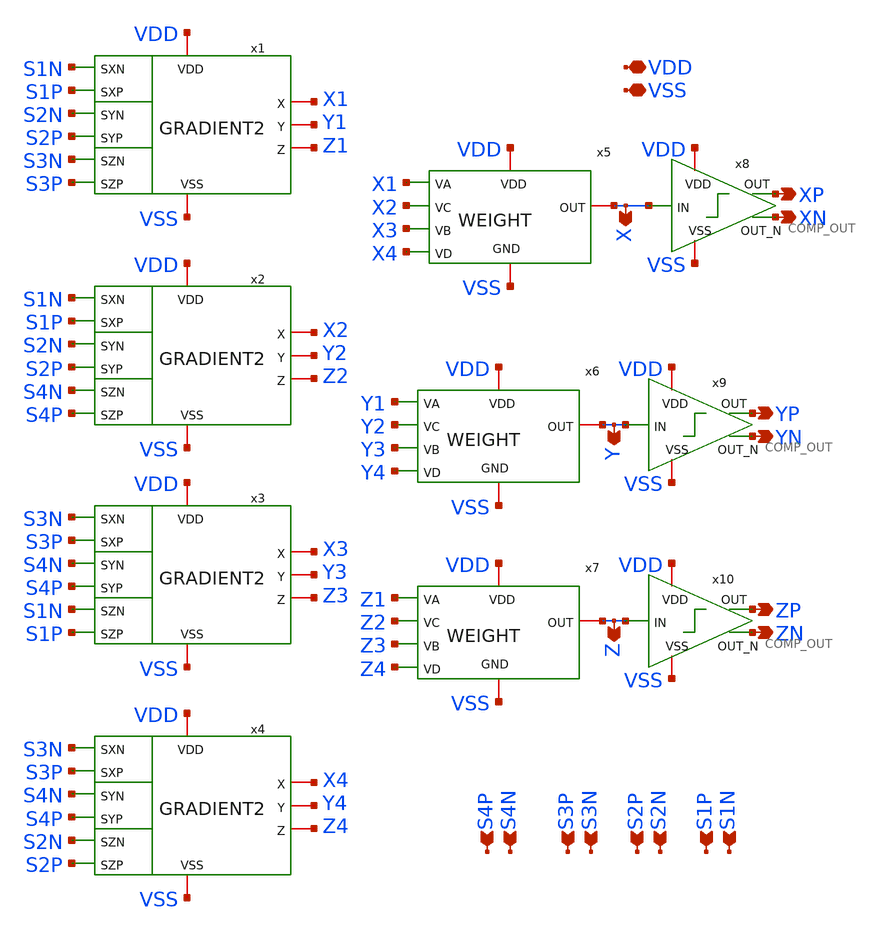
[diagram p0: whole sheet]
** sch_path: FINAL/XSCHEM/GRADIENT_NAV2.sch
**.subckt GRADIENT_NAV2 S1N VDD XN VSS S1P S2N S2P S3N S3P S4N S4P XP YN YP ZN ZP X Y Z
*.ipin S1N
*.iopin VDD
*.opin XN
*.iopin VSS
*.ipin S1P
*.ipin S2N
*.ipin S2P
*.ipin S3N
*.ipin S3P
*.ipin S4N
*.ipin S4P
*.opin XP
*.opin YN
*.opin YP
*.opin ZN
*.opin ZP
*.opin X
*.opin Y
*.opin Z
x5 VDD VSS X X1 X2 X3 X4 WEIGHT
x6 VDD VSS Y Y1 Y2 Y3 Y4 WEIGHT
x7 VDD VSS Z Z1 Z2 Z3 Z4 WEIGHT
x8 VDD XP X XN VSS COMP_OUT
x9 VDD YP Y YN VSS COMP_OUT
x10 VDD ZP Z ZN VSS COMP_OUT
x1 S1N S1P VDD X1 S2N Y1 Z1 S2P VSS S3N S3P GRADIENT2
x2 S1N S1P VDD X2 S2N Y2 Z2 S2P VSS S4N S4P GRADIENT2
x3 S3N S3P VDD X3 S4N Y3 Z3 S4P VSS S1N S1P GRADIENT2
x4 S3N S3P VDD X4 S4N Y4 Z4 S4P VSS S2N S2P GRADIENT2
**** begin user architecture code


* Condensadores de desacople: NMOS y PMOS en inversion metidos en
* los huecos entre macros. LO ESCRIBE scripts/decap_fill.py -- no
* se edita a mano: tiene que ser exactamente lo que hay en el GDS.
XMdecn0 VSS VDD VSS VSS nfet_06v0 L=2.0u W=1.5u nf=1 m=1
XMdecn1 VSS VDD VSS VSS nfet_06v0 L=2.0u W=1.5u nf=1 m=1
XMdecn2 VSS VDD VSS VSS nfet_06v0 L=2.0u W=1.5u nf=1 m=1
XMdecn3 VSS VDD VSS VSS nfet_06v0 L=2.0u W=1.5u nf=1 m=1
XMdecn4 VSS VDD VSS VSS nfet_06v0 L=2.0u W=1.5u nf=1 m=1
XMdecn5 VSS VDD VSS VSS nfet_06v0 L=2.0u W=1.5u nf=1 m=1
XMdecn6 VSS VDD VSS VSS nfet_06v0 L=2.0u W=1.5u nf=1 m=1
XMdecn7 VSS VDD VSS VSS nfet_06v0 L=2.0u W=1.5u nf=1 m=1
XMdecn8 VSS VDD VSS VSS nfet_06v0 L=2.0u W=1.5u nf=1 m=1
XMdecn9 VSS VDD VSS VSS nfet_06v0 L=2.0u W=1.5u nf=1 m=1
XMdecn10 VSS VDD VSS VSS nfet_06v0 L=2.0u W=1.5u nf=1 m=1
XMdecn11 VSS VDD VSS VSS nfet_06v0 L=2.0u W=1.5u nf=1 m=1
XMdecn12 VSS VDD VSS VSS nfet_06v0 L=2.0u W=1.5u nf=1 m=1
XMdecn13 VSS VDD VSS VSS nfet_06v0 L=2.0u W=1.5u nf=1 m=1
XMdecn14 VSS VDD VSS VSS nfet_06v0 L=2.0u W=1.5u nf=1 m=1
XMdecn15 VSS VDD VSS VSS nfet_06v0 L=2.0u W=1.5u nf=1 m=1
XMdecn16 VSS VDD VSS VSS nfet_06v0 L=2.0u W=1.5u nf=1 m=1
XMdecn17 VSS VDD VSS VSS nfet_06v0 L=2.0u W=1.5u nf=1 m=1
XMdecn18 VSS VDD VSS VSS nfet_06v0 L=2.0u W=1.5u nf=1 m=1
XMdecn19 VSS VDD VSS VSS nfet_06v0 L=2.0u W=1.5u nf=1 m=1
XMdecn20 VSS VDD VSS VSS nfet_06v0 L=2.0u W=1.5u nf=1 m=1
XMdecn21 VSS VDD VSS VSS nfet_06v0 L=2.0u W=1.5u nf=1 m=1
XMdecn22 VSS VDD VSS VSS nfet_06v0 L=2.0u W=1.5u nf=1 m=1
XMdecn23 VSS VDD VSS VSS nfet_06v0 L=2.0u W=1.5u nf=1 m=1
XMdecn24 VSS VDD VSS VSS nfet_06v0 L=2.0u W=1.5u nf=1 m=1
XMdecn25 VSS VDD VSS VSS nfet_06v0 L=2.0u W=1.5u nf=1 m=1
XMdecn26 VSS VDD VSS VSS nfet_06v0 L=2.0u W=1.5u nf=1 m=1
XMdecn27 VSS VDD VSS VSS nfet_06v0 L=2.0u W=1.5u nf=1 m=1
XMdecn28 VSS VDD VSS VSS nfet_06v0 L=2.0u W=1.5u nf=1 m=1
XMdecn29 VSS VDD VSS VSS nfet_06v0 L=2.0u W=1.5u nf=1 m=1
XMdecn30 VSS VDD VSS VSS nfet_06v0 L=2.0u W=1.5u nf=1 m=1
XMdecn31 VSS VDD VSS VSS nfet_06v0 L=2.0u W=1.5u nf=1 m=1
XMdecn32 VSS VDD VSS VSS nfet_06v0 L=2.0u W=1.5u nf=1 m=1
XMdecn33 VSS VDD VSS VSS nfet_06v0 L=2.0u W=1.5u nf=1 m=1
XMdecn34 VSS VDD VSS VSS nfet_06v0 L=2.0u W=1.5u nf=1 m=1
XMdecn35 VSS VDD VSS VSS nfet_06v0 L=2.0u W=1.5u nf=1 m=1
XMdecn36 VSS VDD VSS VSS nfet_06v0 L=2.0u W=1.5u nf=1 m=1
XMdecn37 VSS VDD VSS VSS nfet_06v0 L=2.0u W=1.5u nf=1 m=1
XMdecn38 VSS VDD VSS VSS nfet_06v0 L=2.0u W=1.5u nf=1 m=1
XMdecn39 VSS VDD VSS VSS nfet_06v0 L=2.0u W=1.5u nf=1 m=1
XMdecn40 VSS VDD VSS VSS nfet_06v0 L=2.0u W=1.5u nf=1 m=1
XMdecn41 VSS VDD VSS VSS nfet_06v0 L=2.0u W=1.5u nf=1 m=1
XMdecn42 VSS VDD VSS VSS nfet_06v0 L=2.0u W=1.5u nf=1 m=1
XMdecn43 VSS VDD VSS VSS nfet_06v0 L=2.0u W=1.5u nf=1 m=1
XMdecn44 VSS VDD VSS VSS nfet_06v0 L=2.0u W=1.5u nf=1 m=1
XMdecn45 VSS VDD VSS VSS nfet_06v0 L=2.0u W=1.5u nf=1 m=1
XMdecn46 VSS VDD VSS VSS nfet_06v0 L=2.0u W=1.5u nf=1 m=1
XMdecn47 VSS VDD VSS VSS nfet_06v0 L=2.0u W=1.5u nf=1 m=1
XMdecn48 VSS VDD VSS VSS nfet_06v0 L=2.0u W=1.5u nf=1 m=1
XMdecn49 VSS VDD VSS VSS nfet_06v0 L=2.0u W=1.5u nf=1 m=1
XMdecn50 VSS VDD VSS VSS nfet_06v0 L=2.0u W=1.5u nf=1 m=1
XMdecn51 VSS VDD VSS VSS nfet_06v0 L=2.0u W=1.5u nf=1 m=1
XMdecn52 VSS VDD VSS VSS nfet_06v0 L=2.0u W=1.5u nf=1 m=1
XMdecp53 VDD VSS VDD VDD pfet_06v0 L=2.0u W=1.5u nf=1 m=1
XMdecp54 VDD VSS VDD VDD pfet_06v0 L=2.0u W=1.5u nf=1 m=1
XMdecp55 VDD VSS VDD VDD pfet_06v0 L=2.0u W=1.5u nf=1 m=1
XMdecp56 VDD VSS VDD VDD pfet_06v0 L=2.0u W=1.5u nf=1 m=1
XMdecp57 VDD VSS VDD VDD pfet_06v0 L=2.0u W=1.5u nf=1 m=1
XMdecp58 VDD VSS VDD VDD pfet_06v0 L=2.0u W=1.5u nf=1 m=1
XMdecp59 VDD VSS VDD VDD pfet_06v0 L=2.0u W=1.5u nf=1 m=1
XMdecp60 VDD VSS VDD VDD pfet_06v0 L=2.0u W=1.5u nf=1 m=1
XMdecp61 VDD VSS VDD VDD pfet_06v0 L=2.0u W=1.5u nf=1 m=1
XMdecp62 VDD VSS VDD VDD pfet_06v0 L=2.0u W=1.5u nf=1 m=1
XMdecp63 VDD VSS VDD VDD pfet_06v0 L=2.0u W=1.5u nf=1 m=1
XMdecp64 VDD VSS VDD VDD pfet_06v0 L=2.0u W=1.5u nf=1 m=1
XMdecp65 VDD VSS VDD VDD pfet_06v0 L=2.0u W=1.5u nf=1 m=1
XMdecp66 VDD VSS VDD VDD pfet_06v0 L=2.0u W=1.5u nf=1 m=1
XMdecp67 VDD VSS VDD VDD pfet_06v0 L=2.0u W=1.5u nf=1 m=1
XMdecp68 VDD VSS VDD VDD pfet_06v0 L=2.0u W=1.5u nf=1 m=1
XMdecp69 VDD VSS VDD VDD pfet_06v0 L=2.0u W=1.5u nf=1 m=1
XMdecp70 VDD VSS VDD VDD pfet_06v0 L=2.0u W=1.5u nf=1 m=1
XMdecp71 VDD VSS VDD VDD pfet_06v0 L=2.0u W=1.5u nf=1 m=1
XMdecp72 VDD VSS VDD VDD pfet_06v0 L=2.0u W=1.5u nf=1 m=1
XMdecp73 VDD VSS VDD VDD pfet_06v0 L=2.0u W=1.5u nf=1 m=1
XMdecp74 VDD VSS VDD VDD pfet_06v0 L=2.0u W=1.5u nf=1 m=1
XMdecp75 VDD VSS VDD VDD pfet_06v0 L=2.0u W=1.5u nf=1 m=1
XMdecp76 VDD VSS VDD VDD pfet_06v0 L=2.0u W=1.5u nf=1 m=1
XMdecp77 VDD VSS VDD VDD pfet_06v0 L=2.0u W=1.5u nf=1 m=1
XMdecp78 VDD VSS VDD VDD pfet_06v0 L=2.0u W=1.5u nf=1 m=1
XMdecp79 VDD VSS VDD VDD pfet_06v0 L=2.0u W=1.5u nf=1 m=1
XMdecp80 VDD VSS VDD VDD pfet_06v0 L=2.0u W=1.5u nf=1 m=1
XMdecp81 VDD VSS VDD VDD pfet_06v0 L=2.0u W=1.5u nf=1 m=1
XMdecp82 VDD VSS VDD VDD pfet_06v0 L=2.0u W=1.5u nf=1 m=1
XMdecp83 VDD VSS VDD VDD pfet_06v0 L=2.0u W=1.5u nf=1 m=1
XMdecp84 VDD VSS VDD VDD pfet_06v0 L=2.0u W=1.5u nf=1 m=1
XMdecp85 VDD VSS VDD VDD pfet_06v0 L=2.0u W=1.5u nf=1 m=1
XMdecp86 VDD VSS VDD VDD pfet_06v0 L=2.0u W=1.5u nf=1 m=1
XMdecp87 VDD VSS VDD VDD pfet_06v0 L=2.0u W=1.5u nf=1 m=1
XMdecp88 VDD VSS VDD VDD pfet_06v0 L=2.0u W=1.5u nf=1 m=1
XMdecp89 VDD VSS VDD VDD pfet_06v0 L=2.0u W=1.5u nf=1 m=1
XMdecp90 VDD VSS VDD VDD pfet_06v0 L=2.0u W=1.5u nf=1 m=1
XMdecp91 VDD VSS VDD VDD pfet_06v0 L=2.0u W=1.5u nf=1 m=1
XMdecp92 VDD VSS VDD VDD pfet_06v0 L=2.0u W=1.5u nf=1 m=1
XMdecp93 VDD VSS VDD VDD pfet_06v0 L=2.0u W=1.5u nf=1 m=1
XMdecp94 VDD VSS VDD VDD pfet_06v0 L=2.0u W=1.5u nf=1 m=1
XMdecp95 VDD VSS VDD VDD pfet_06v0 L=2.0u W=1.5u nf=1 m=1
XMdecp96 VDD VSS VDD VDD pfet_06v0 L=2.0u W=1.5u nf=1 m=1
XMdecp97 VDD VSS VDD VDD pfet_06v0 L=2.0u W=1.5u nf=1 m=1
XMdecp98 VDD VSS VDD VDD pfet_06v0 L=2.0u W=1.5u nf=1 m=1
XMdecp99 VDD VSS VDD VDD pfet_06v0 L=2.0u W=1.5u nf=1 m=1
XMdecp100 VDD VSS VDD VDD pfet_06v0 L=2.0u W=1.5u nf=1 m=1
XMdecp101 VDD VSS VDD VDD pfet_06v0 L=2.0u W=1.5u nf=1 m=1
XMdecn102 VSS VDD VSS VSS nfet_06v0 L=2.0u W=18.0u nf=1 m=1
XMdecn103 VSS VDD VSS VSS nfet_06v0 L=2.0u W=18.0u nf=1 m=1
XMdecp104 VDD VSS VDD VDD pfet_06v0 L=2.0u W=18.0u nf=1 m=1
XMdecp105 VDD VSS VDD VDD pfet_06v0 L=2.0u W=18.0u nf=1 m=1
XMdecn106 VSS VDD VSS VSS nfet_06v0 L=2.0u W=18.0u nf=1 m=1
XMdecn107 VSS VDD VSS VSS nfet_06v0 L=2.0u W=18.0u nf=1 m=1
XMdecp108 VDD VSS VDD VDD pfet_06v0 L=2.0u W=18.0u nf=1 m=1
XMdecp109 VDD VSS VDD VDD pfet_06v0 L=2.0u W=18.0u nf=1 m=1
XMdecn110 VSS VDD VSS VSS nfet_06v0 L=2.0u W=18.0u nf=1 m=1
XMdecn111 VSS VDD VSS VSS nfet_06v0 L=2.0u W=18.0u nf=1 m=1
XMdecp112 VDD VSS VDD VDD pfet_06v0 L=2.0u W=18.0u nf=1 m=1
XMdecp113 VDD VSS VDD VDD pfet_06v0 L=2.0u W=18.0u nf=1 m=1
XMdecn114 VSS VDD VSS VSS nfet_06v0 L=2.0u W=18.0u nf=1 m=1
XMdecn115 VSS VDD VSS VSS nfet_06v0 L=2.0u W=18.0u nf=1 m=1
XMdecp116 VDD VSS VDD VDD pfet_06v0 L=2.0u W=18.0u nf=1 m=1
XMdecp117 VDD VSS VDD VDD pfet_06v0 L=2.0u W=18.0u nf=1 m=1
XMdecn118 VSS VDD VSS VSS nfet_06v0 L=2.0u W=18.0u nf=1 m=1
XMdecn119 VSS VDD VSS VSS nfet_06v0 L=2.0u W=18.0u nf=1 m=1
XMdecp120 VDD VSS VDD VDD pfet_06v0 L=2.0u W=18.0u nf=1 m=1
XMdecp121 VDD VSS VDD VDD pfet_06v0 L=2.0u W=18.0u nf=1 m=1
XMdecn122 VSS VDD VSS VSS nfet_06v0 L=2.0u W=18.0u nf=1 m=1
XMdecn123 VSS VDD VSS VSS nfet_06v0 L=2.0u W=18.0u nf=1 m=1
XMdecp124 VDD VSS VDD VDD pfet_06v0 L=2.0u W=18.0u nf=1 m=1
XMdecp125 VDD VSS VDD VDD pfet_06v0 L=2.0u W=18.0u nf=1 m=1
XMdecn126 VSS VDD VSS VSS nfet_06v0 L=2.0u W=18.0u nf=1 m=1
XMdecn127 VSS VDD VSS VSS nfet_06v0 L=2.0u W=18.0u nf=1 m=1
XMdecp128 VDD VSS VDD VDD pfet_06v0 L=2.0u W=18.0u nf=1 m=1
XMdecp129 VDD VSS VDD VDD pfet_06v0 L=2.0u W=18.0u nf=1 m=1
XMdecn130 VSS VDD VSS VSS nfet_06v0 L=2.0u W=18.0u nf=1 m=1
XMdecn131 VSS VDD VSS VSS nfet_06v0 L=2.0u W=18.0u nf=1 m=1
XMdecp132 VDD VSS VDD VDD pfet_06v0 L=2.0u W=18.0u nf=1 m=1
XMdecp133 VDD VSS VDD VDD pfet_06v0 L=2.0u W=18.0u nf=1 m=1
XMdecn134 VSS VDD VSS VSS nfet_06v0 L=2.0u W=18.0u nf=1 m=1
XMdecn135 VSS VDD VSS VSS nfet_06v0 L=2.0u W=18.0u nf=1 m=1
XMdecp136 VDD VSS VDD VDD pfet_06v0 L=2.0u W=18.0u nf=1 m=1
XMdecp137 VDD VSS VDD VDD pfet_06v0 L=2.0u W=18.0u nf=1 m=1
XMdecn138 VSS VDD VSS VSS nfet_06v0 L=2.0u W=18.0u nf=1 m=1
XMdecp139 VDD VSS VDD VDD pfet_06v0 L=2.0u W=18.0u nf=1 m=1
XMdecn140 VSS VDD VSS VSS nfet_06v0 L=2.0u W=18.0u nf=1 m=1
XMdecp141 VDD VSS VDD VDD pfet_06v0 L=2.0u W=18.0u nf=1 m=1
XMdecn142 VSS VDD VSS VSS nfet_06v0 L=2.0u W=18.0u nf=1 m=1
XMdecp143 VDD VSS VDD VDD pfet_06v0 L=2.0u W=18.0u nf=1 m=1
XMdecn144 VSS VDD VSS VSS nfet_06v0 L=2.0u W=9.75u nf=1 m=1
XMdecn145 VSS VDD VSS VSS nfet_06v0 L=2.0u W=9.75u nf=1 m=1
XMdecp146 VDD VSS VDD VDD pfet_06v0 L=2.0u W=9.75u nf=1 m=1
XMdecp147 VDD VSS VDD VDD pfet_06v0 L=2.0u W=9.75u nf=1 m=1
XMdecn148 VSS VDD VSS VSS nfet_06v0 L=2.0u W=9.75u nf=1 m=1
XMdecn149 VSS VDD VSS VSS nfet_06v0 L=2.0u W=9.75u nf=1 m=1
XMdecp150 VDD VSS VDD VDD pfet_06v0 L=2.0u W=9.75u nf=1 m=1
XMdecp151 VDD VSS VDD VDD pfet_06v0 L=2.0u W=9.75u nf=1 m=1
XMdecn152 VSS VDD VSS VSS nfet_06v0 L=2.0u W=9.75u nf=1 m=1
XMdecn153 VSS VDD VSS VSS nfet_06v0 L=2.0u W=9.75u nf=1 m=1
XMdecp154 VDD VSS VDD VDD pfet_06v0 L=2.0u W=9.75u nf=1 m=1
XMdecp155 VDD VSS VDD VDD pfet_06v0 L=2.0u W=9.75u nf=1 m=1
XMdecn156 VSS VDD VSS VSS nfet_06v0 L=2.0u W=9.75u nf=1 m=1
XMdecn157 VSS VDD VSS VSS nfet_06v0 L=2.0u W=9.75u nf=1 m=1
XMdecp158 VDD VSS VDD VDD pfet_06v0 L=2.0u W=9.75u nf=1 m=1
XMdecp159 VDD VSS VDD VDD pfet_06v0 L=2.0u W=9.75u nf=1 m=1
XMdecn160 VSS VDD VSS VSS nfet_06v0 L=2.0u W=9.75u nf=1 m=1
XMdecn161 VSS VDD VSS VSS nfet_06v0 L=2.0u W=9.75u nf=1 m=1
XMdecp162 VDD VSS VDD VDD pfet_06v0 L=2.0u W=9.75u nf=1 m=1
XMdecp163 VDD VSS VDD VDD pfet_06v0 L=2.0u W=9.75u nf=1 m=1
XMdecn164 VSS VDD VSS VSS nfet_06v0 L=2.0u W=9.75u nf=1 m=1
XMdecn165 VSS VDD VSS VSS nfet_06v0 L=2.0u W=9.75u nf=1 m=1
XMdecp166 VDD VSS VDD VDD pfet_06v0 L=2.0u W=9.75u nf=1 m=1
XMdecp167 VDD VSS VDD VDD pfet_06v0 L=2.0u W=9.75u nf=1 m=1
XMdecn168 VSS VDD VSS VSS nfet_06v0 L=2.0u W=9.75u nf=1 m=1
XMdecn169 VSS VDD VSS VSS nfet_06v0 L=2.0u W=9.75u nf=1 m=1
XMdecp170 VDD VSS VDD VDD pfet_06v0 L=2.0u W=9.75u nf=1 m=1
XMdecp171 VDD VSS VDD VDD pfet_06v0 L=2.0u W=9.75u nf=1 m=1
XMdecn172 VSS VDD VSS VSS nfet_06v0 L=2.0u W=9.75u nf=1 m=1
XMdecn173 VSS VDD VSS VSS nfet_06v0 L=2.0u W=9.75u nf=1 m=1
XMdecp174 VDD VSS VDD VDD pfet_06v0 L=2.0u W=9.75u nf=1 m=1
XMdecp175 VDD VSS VDD VDD pfet_06v0 L=2.0u W=9.75u nf=1 m=1
XMdecn176 VSS VDD VSS VSS nfet_06v0 L=2.0u W=9.75u nf=1 m=1
XMdecn177 VSS VDD VSS VSS nfet_06v0 L=2.0u W=9.75u nf=1 m=1
XMdecp178 VDD VSS VDD VDD pfet_06v0 L=2.0u W=9.75u nf=1 m=1
XMdecp179 VDD VSS VDD VDD pfet_06v0 L=2.0u W=9.75u nf=1 m=1
XMdecn180 VSS VDD VSS VSS nfet_06v0 L=2.0u W=9.75u nf=1 m=1
XMdecn181 VSS VDD VSS VSS nfet_06v0 L=2.0u W=9.75u nf=1 m=1
XMdecp182 VDD VSS VDD VDD pfet_06v0 L=2.0u W=9.75u nf=1 m=1
XMdecp183 VDD VSS VDD VDD pfet_06v0 L=2.0u W=9.75u nf=1 m=1
XMdecn184 VSS VDD VSS VSS nfet_06v0 L=2.0u W=9.75u nf=1 m=1
XMdecn185 VSS VDD VSS VSS nfet_06v0 L=2.0u W=9.75u nf=1 m=1
XMdecp186 VDD VSS VDD VDD pfet_06v0 L=2.0u W=9.75u nf=1 m=1
XMdecp187 VDD VSS VDD VDD pfet_06v0 L=2.0u W=9.75u nf=1 m=1
XMdecn188 VSS VDD VSS VSS nfet_06v0 L=2.0u W=9.75u nf=1 m=1
XMdecn189 VSS VDD VSS VSS nfet_06v0 L=2.0u W=9.75u nf=1 m=1
XMdecp190 VDD VSS VDD VDD pfet_06v0 L=2.0u W=9.75u nf=1 m=1
XMdecp191 VDD VSS VDD VDD pfet_06v0 L=2.0u W=9.75u nf=1 m=1
XMdecn192 VSS VDD VSS VSS nfet_06v0 L=2.0u W=18.0u nf=1 m=1
XMdecp193 VDD VSS VDD VDD pfet_06v0 L=2.0u W=18.0u nf=1 m=1
XMdecn194 VSS VDD VSS VSS nfet_06v0 L=2.0u W=18.0u nf=1 m=1
XMdecp195 VDD VSS VDD VDD pfet_06v0 L=2.0u W=18.0u nf=1 m=1
XMdecn196 VSS VDD VSS VSS nfet_06v0 L=2.0u W=18.0u nf=1 m=1
XMdecp197 VDD VSS VDD VDD pfet_06v0 L=2.0u W=18.0u nf=1 m=1
XMdecn198 VSS VDD VSS VSS nfet_06v0 L=2.0u W=1.5u nf=1 m=1
XMdecn199 VSS VDD VSS VSS nfet_06v0 L=2.0u W=1.5u nf=1 m=1
XMdecn200 VSS VDD VSS VSS nfet_06v0 L=2.0u W=1.5u nf=1 m=1
XMdecn201 VSS VDD VSS VSS nfet_06v0 L=2.0u W=1.5u nf=1 m=1
XMdecp202 VDD VSS VDD VDD pfet_06v0 L=2.0u W=1.5u nf=1 m=1
XMdecp203 VDD VSS VDD VDD pfet_06v0 L=2.0u W=1.5u nf=1 m=1
XMdecp204 VDD VSS VDD VDD pfet_06v0 L=2.0u W=1.5u nf=1 m=1
XMdecp205 VDD VSS VDD VDD pfet_06v0 L=2.0u W=1.5u nf=1 m=1
XMdecn206 VSS VDD VSS VSS nfet_06v0 L=2.0u W=9.75u nf=1 m=1
XMdecp207 VDD VSS VDD VDD pfet_06v0 L=2.0u W=9.75u nf=1 m=1
XMdecn208 VSS VDD VSS VSS nfet_06v0 L=2.0u W=9.75u nf=1 m=1
XMdecp209 VDD VSS VDD VDD pfet_06v0 L=2.0u W=9.75u nf=1 m=1
XMdecn210 VSS VDD VSS VSS nfet_06v0 L=2.0u W=9.75u nf=1 m=1
XMdecp211 VDD VSS VDD VDD pfet_06v0 L=2.0u W=9.75u nf=1 m=1
XMdecn212 VSS VDD VSS VSS nfet_06v0 L=2.0u W=9.75u nf=1 m=1
XMdecp213 VDD VSS VDD VDD pfet_06v0 L=2.0u W=9.75u nf=1 m=1
XMdecn214 VSS VDD VSS VSS nfet_06v0 L=2.0u W=1.5u nf=1 m=1
XMdecn215 VSS VDD VSS VSS nfet_06v0 L=2.0u W=1.5u nf=1 m=1
XMdecp216 VDD VSS VDD VDD pfet_06v0 L=2.0u W=1.5u nf=1 m=1
XMdecp217 VDD VSS VDD VDD pfet_06v0 L=2.0u W=1.5u nf=1 m=1
XMdecn218 VSS VDD VSS VSS nfet_06v0 L=2.0u W=1.5u nf=1 m=1
XMdecn219 VSS VDD VSS VSS nfet_06v0 L=2.0u W=1.5u nf=1 m=1
XMdecp220 VDD VSS VDD VDD pfet_06v0 L=2.0u W=1.5u nf=1 m=1
XMdecp221 VDD VSS VDD VDD pfet_06v0 L=2.0u W=1.5u nf=1 m=1
XMdecn222 VSS VDD VSS VSS nfet_06v0 L=2.0u W=1.5u nf=1 m=1
XMdecp223 VDD VSS VDD VDD pfet_06v0 L=2.0u W=1.5u nf=1 m=1


**** end user architecture code
**.ends
.end
